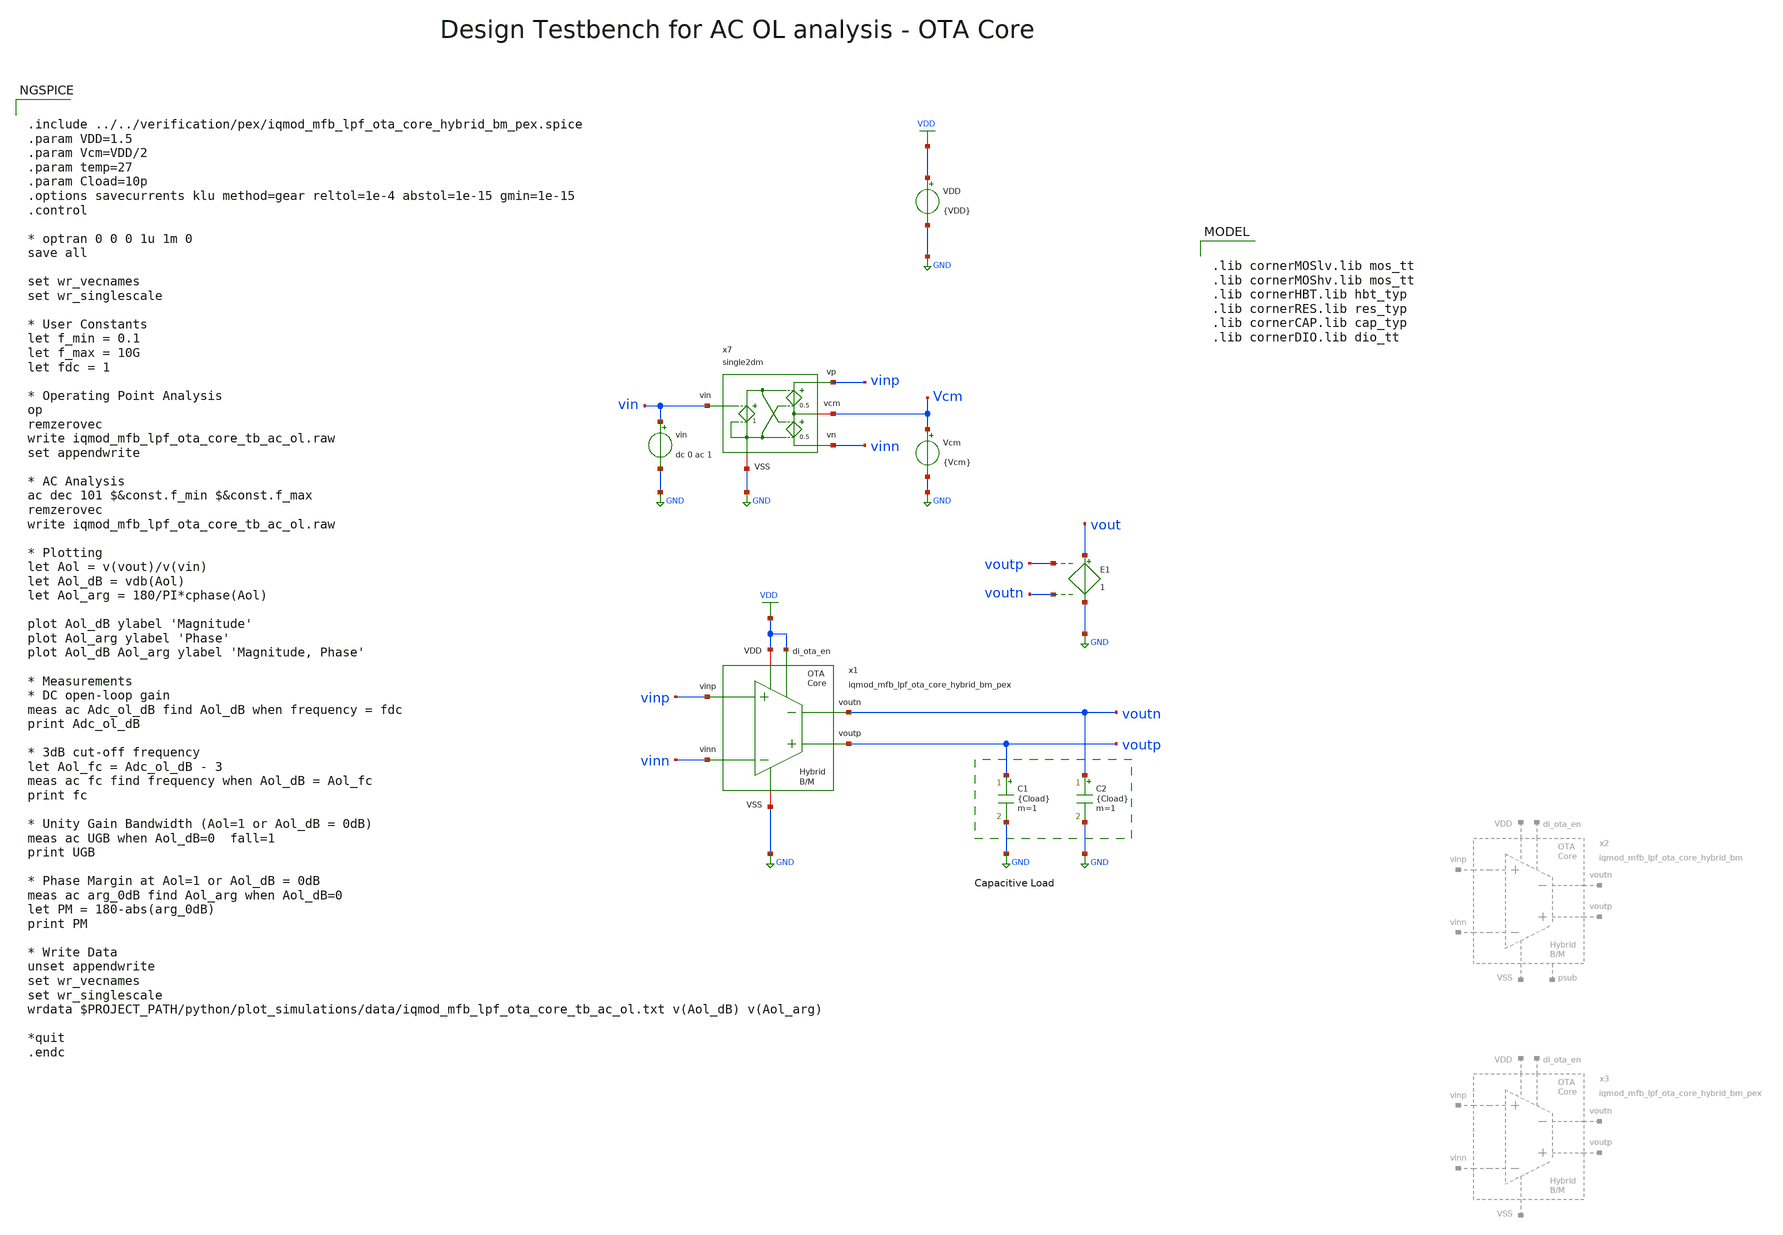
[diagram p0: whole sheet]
** sch_path: ihp130/macros/iqmod/xschem/testbenches/iqmod_mfb_lpf_ota_core_tb_ac_ol.sch
**.subckt iqmod_mfb_lpf_ota_core_tb_ac_ol
VDD VDD GND {VDD}
C1 voutp GND {Cload} m=1
C2 voutn GND {Cload} m=1
E1 vout GND voutp voutn 1
vin vin GND dc 0 ac 1
x7 vinp vin Vcm GND vinn single2dm
Vcm Vcm GND {Vcm}
x1 voutp voutn vinn vinp VDD GND VDD iqmod_mfb_lpf_ota_core_hybrid_bm_pex
**** begin user architecture code


.include ../../verification/pex/iqmod_mfb_lpf_ota_core_hybrid_bm_pex.spice
.param VDD=1.5
.param Vcm=VDD/2
.param temp=27
.param Cload=10p
.options savecurrents klu method=gear reltol=1e-4 abstol=1e-15 gmin=1e-15
.control

* optran 0 0 0 1u 1m 0
save all

set wr_vecnames
set wr_singlescale

* User Constants
let f_min = 0.1
let f_max = 10G
let fdc = 1

* Operating Point Analysis
op
remzerovec
write iqmod_mfb_lpf_ota_core_tb_ac_ol.raw
set appendwrite

* AC Analysis
ac dec 101 $&const.f_min $&const.f_max
remzerovec
write iqmod_mfb_lpf_ota_core_tb_ac_ol.raw

* Plotting
let Aol = v(vout)/v(vin)
let Aol_dB = vdb(Aol)
let Aol_arg = 180/PI*cphase(Aol)

plot Aol_dB ylabel 'Magnitude'
plot Aol_arg ylabel 'Phase'
plot Aol_dB Aol_arg ylabel 'Magnitude, Phase'

* Measurements
* DC open-loop gain
meas ac Adc_ol_dB find Aol_dB when frequency = fdc
print Adc_ol_dB

* 3dB cut-off frequency
let Aol_fc = Adc_ol_dB - 3
meas ac fc find frequency when Aol_dB = Aol_fc
print fc

* Unity Gain Bandwidth (Aol=1 or Aol_dB = 0dB)
meas ac UGB when Aol_dB=0  fall=1
print UGB

* Phase Margin at Aol=1 or Aol_dB = 0dB
meas ac arg_0dB find Aol_arg when Aol_dB=0
let PM = 180-abs(arg_0dB)
print PM

* Write Data
unset appendwrite
set wr_vecnames
set wr_singlescale
wrdata $PROJECT_PATH/python/plot_simulations/data/iqmod_mfb_lpf_ota_core_tb_ac_ol.txt v(Aol_dB)
+ v(Aol_arg)

*quit
.endc



.lib cornerMOSlv.lib mos_tt
.lib cornerMOShv.lib mos_tt
.lib cornerHBT.lib hbt_typ
.lib cornerRES.lib res_typ
.lib cornerCAP.lib cap_typ
.lib cornerDIO.lib dio_tt

**** end user architecture code
**.ends
.GLOBAL GND
.GLOBAL VDD
.end
